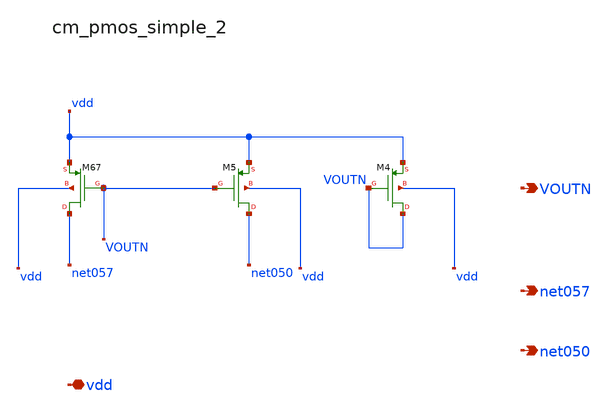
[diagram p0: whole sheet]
** sch_path: analog-db/raw/amp_021_yan_az/hier/blocks/cm_pmos_simple_2.sch
**.subckt cm_pmos_simple_2 vdd VOUTN net057 net050
*.iopin vdd
*.opin VOUTN
*.opin net057
*.opin net050
XM4 VOUTN VOUTN vdd vdd sg13_lv_pmos w=x_dut_xm4_w l=x_dut_xm4_l ng=1 m=x_dut_xm4_m
XM5 net050 VOUTN vdd vdd sg13_lv_pmos w=x_dut_xm5_w l=x_dut_xm5_l ng=1 m=x_dut_xm5_m
XM67 net057 VOUTN vdd vdd sg13_lv_pmos w=x_dut_xm67_w l=x_dut_xm67_l ng=1 m=x_dut_xm67_m
**.ends
.end
